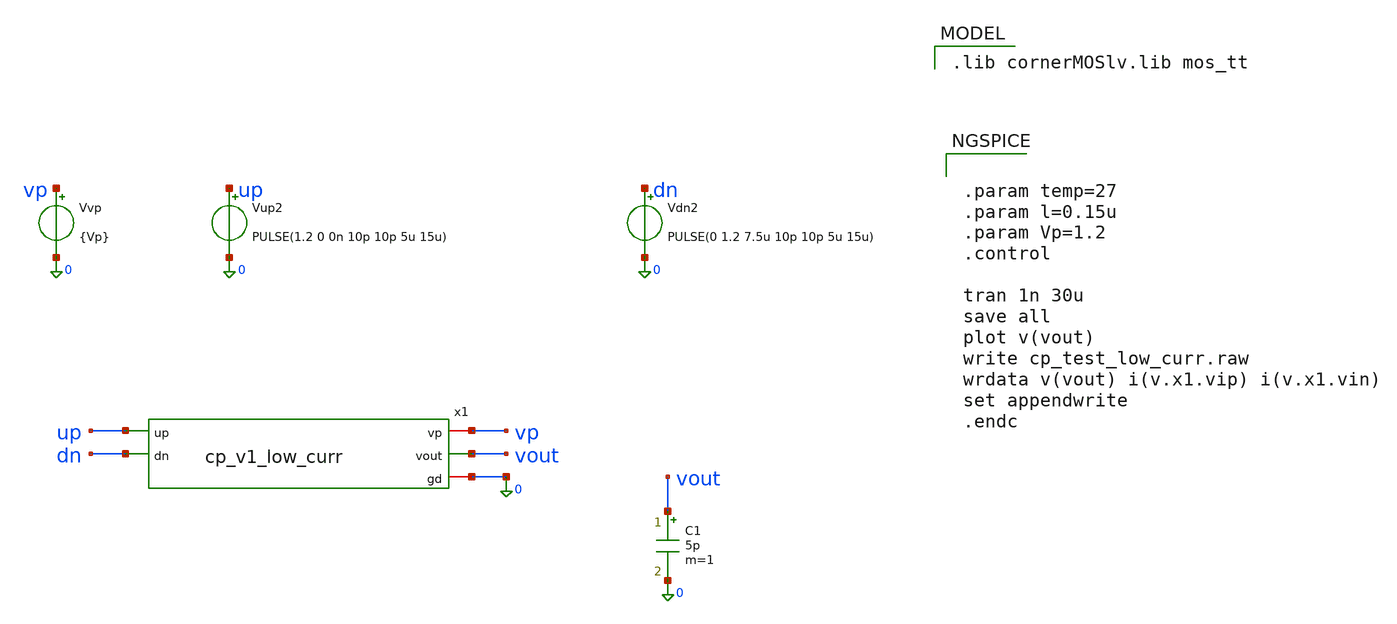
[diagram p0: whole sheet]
** sch_path: schematics/charge_pump/cp_v1_low_curr_tb.sch
**.subckt cp_v1_low_curr_tb
Vvp vp 0 {Vp}
C1 vout 0 5p m=1
Vup2 up 0 PULSE(1.2 0 0n 10p 10p 5u 15u)
Vdn2 dn 0 PULSE(0 1.2 7.5u 10p 10p 5u 15u)
x1 vp up vout dn 0 cp_v1_low_curr
**** begin user architecture code
 .lib cornerMOSlv.lib mos_tt



.param temp=27
.param l=0.15u
.param Vp=1.2
.control

tran 1n 30u
save all
plot v(vout)
write cp_test_low_curr.raw
wrdata v(vout) i(v.x1.vip) i(v.x1.vin)
set appendwrite
.endc


**** end user architecture code
**.ends

* expanding   symbol:  /foss/designs/CHIP-PLL/charge_pump/cp_v1_low_curr.sym # of pins=5
** sym_path: schematics/charge_pump/cp_v1_low_curr.sym
** sch_path: schematics/charge_pump/cp_v1_low_curr.sch
.subckt cp_v1_low_curr vp up vout dn gd
*.ipin up
*.ipin dn
*.iopin vp
*.iopin gd
*.opin vout
XM7 VH biasp net8 vp sg13_lv_pmos w=1u l=0.15u ng=1 m=3 mm_ok=1
XM12 vout up VH vp sg13_lv_pmos w=1u l=0.15u ng=1 m=1 mm_ok=1
XM14 vout dn VF gd sg13_lv_nmos w=1u l=0.15u ng=1 m=1 mm_ok=1
XM15 net9 biasn net4 gd sg13_lv_nmos w=1u l=0.15u ng=1 m=1 mm_ok=1
XM16 net4 net3 gd gd sg13_lv_nmos w=1u l=0.15u ng=1 m=1 mm_ok=1
XM17 Vn net1 vp vp sg13_lv_pmos w=1u l=0.15u ng=1 m=1 mm_ok=1
XM18 0 vout Vn vp sg13_lv_pmos w=1u l=0.15u ng=1 m=1 mm_ok=1
XM19 vp vout Vp2 gd sg13_lv_nmos w=1u l=0.15u ng=1 m=1 mm_ok=1
XM20 Vp2 net3 gd gd sg13_lv_nmos w=1u l=0.15u ng=1 m=1 mm_ok=1
XM1 net1 Vn VE 0 sg13_lv_nmos w=1u l=0.15u ng=1 m=1 mm_ok=1
XM2 net6 net1 vp vp sg13_lv_pmos w=1u l=0.15u ng=1 m=1 mm_ok=1
XM5 VG biasp net6 vp sg13_lv_pmos w=1u l=0.15u ng=1 m=1 mm_ok=1
XM3 net1 Vp2 VG vp sg13_lv_pmos w=1u l=0.15u ng=1 m=1 mm_ok=1
XM6 VE biasn net7 gd sg13_lv_nmos w=1u l=0.15u ng=1 m=1 mm_ok=1
XM8 net7 net3 gd gd sg13_lv_nmos w=1u l=0.15u ng=1 m=1 mm_ok=1
XM9 net3 biasn net2 gd sg13_lv_nmos w=1u l=0.15u ng=1 m=1 mm_ok=1
XM10 net2 net3 gd gd sg13_lv_nmos w=1u l=0.15u ng=1 m=1 mm_ok=1
Vip net5 net8 0
Vin VF net9 0
XM11 net5 net1 vp vp sg13_lv_pmos w=1u l=0.15u ng=1 m=3 mm_ok=1
Iip1 vp net3 0.5u
Vip1 biasp gd 0.6
Vip2 biasn gd 0.6
.ends

.end
